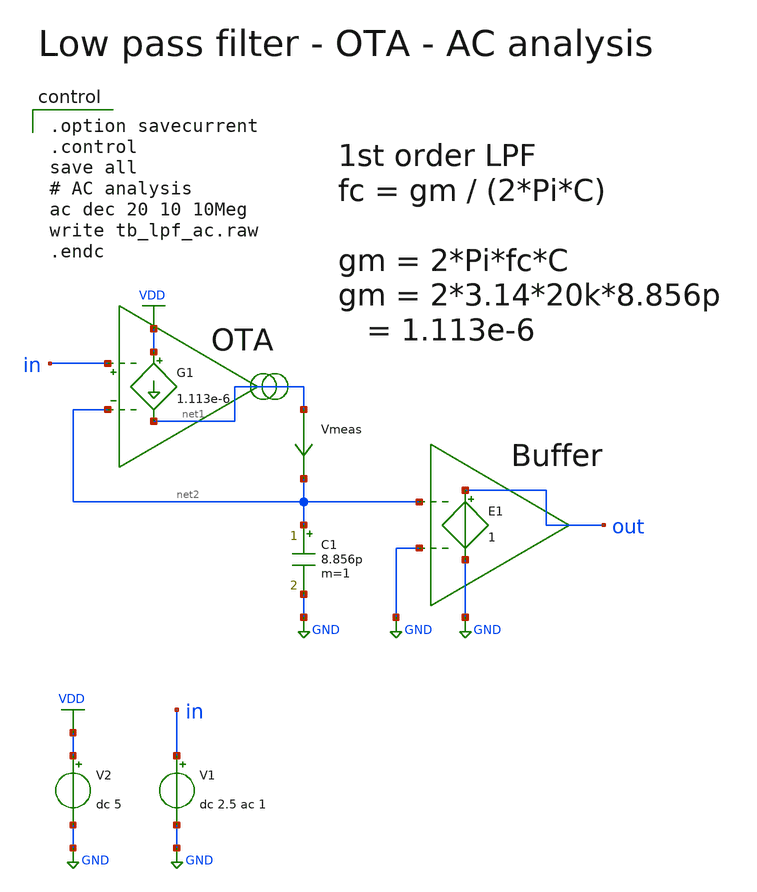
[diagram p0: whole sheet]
** sch_path: member_project/AM_Radio/Yamada3/xschem/tb_lpf_ac.sch
**.subckt tb_lpf_ac
V2 VDD GND dc 5
V1 in GND dc 2.5 ac 1
G1 VDD net1 in net2 1.113e-6
Vmeas net1 net2 0
.save i(vmeas)
C1 net2 GND 8.856p m=1
E1 out GND net2 GND 1
**** begin user architecture code

.option savecurrent
.control
save all
# AC analysis
ac dec 20 10 10Meg
write tb_lpf_ac.raw
.endc

**** end user architecture code
**.ends
.GLOBAL GND
.GLOBAL VDD
.end
